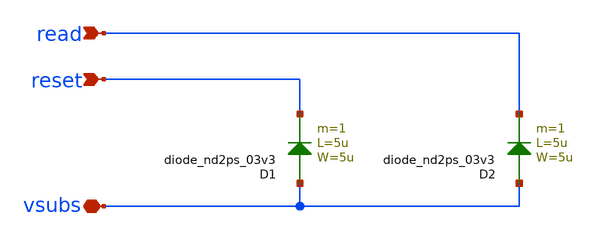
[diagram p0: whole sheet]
** sch_path: xschem/ip_pixel_frame_right.sch
**.subckt ip_pixel_frame_right read reset vsubs
*.ipin read
*.ipin reset
*.iopin vsubs
D1 vsubs reset diode_nd2ps_03v3 area='5u * 5u ' pj='2*5u + 2*5u ' m=1
D2 vsubs read diode_nd2ps_03v3 area='5u * 5u ' pj='2*5u + 2*5u ' m=1
**.ends
.end
